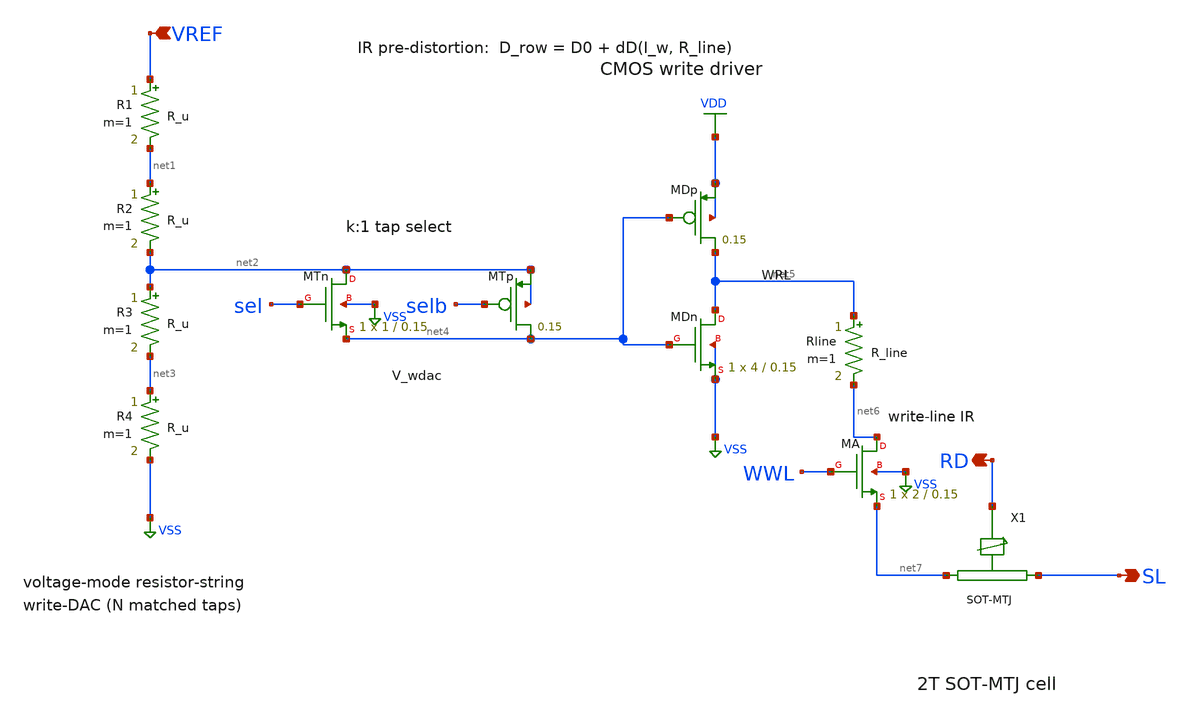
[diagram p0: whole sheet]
** sch_path: eda/hero/schematics/writepath.sch
**.subckt writepath VREF SL RD
*.ipin VREF
*.opin SL
*.opin RD
R1 VREF net1 R_u m=1
R2 net1 net2 R_u m=1
R3 net2 net3 R_u m=1
R4 net3 VSS R_u m=1
XMTn net2 sel net4 VSS sky130_fd_pr__sky130_fd_pr__nfet_01v8 L=0.15 W=1 nrd='0.29 / W' nrs='0.29 / W'
+ sa=0 sb=0 sd=0 mult=1 m=1
XMTp net4 selb net2 net2 sky130_fd_pr__sky130_fd_pr__pfet_01v8 L=0.15 W=2 nrd='0.29 / W' nrs='0.29 / W'
+ sa=0 sb=0 sd=0 mult=1 m=1
XMDp net5 net4 VDD VDD sky130_fd_pr__sky130_fd_pr__pfet_01v8 L=0.15 W=8 nrd='0.29 / W' nrs='0.29 / W'
+ sa=0 sb=0 sd=0 mult=1 m=1
XMDn net5 net4 VSS VSS sky130_fd_pr__sky130_fd_pr__nfet_01v8 L=0.15 W=4 nrd='0.29 / W' nrs='0.29 / W'
+ sa=0 sb=0 sd=0 mult=1 m=1
Rline net5 net6 R_line m=1
XMA net6 WWL net7 VSS sky130_fd_pr__sky130_fd_pr__nfet_01v8 L=0.15 W=2 nrd='0.29 / W' nrs='0.29 / W'
+ sa=0 sb=0 sd=0 mult=1 m=1
**.ends
.GLOBAL VSS
.GLOBAL VDD
.end
